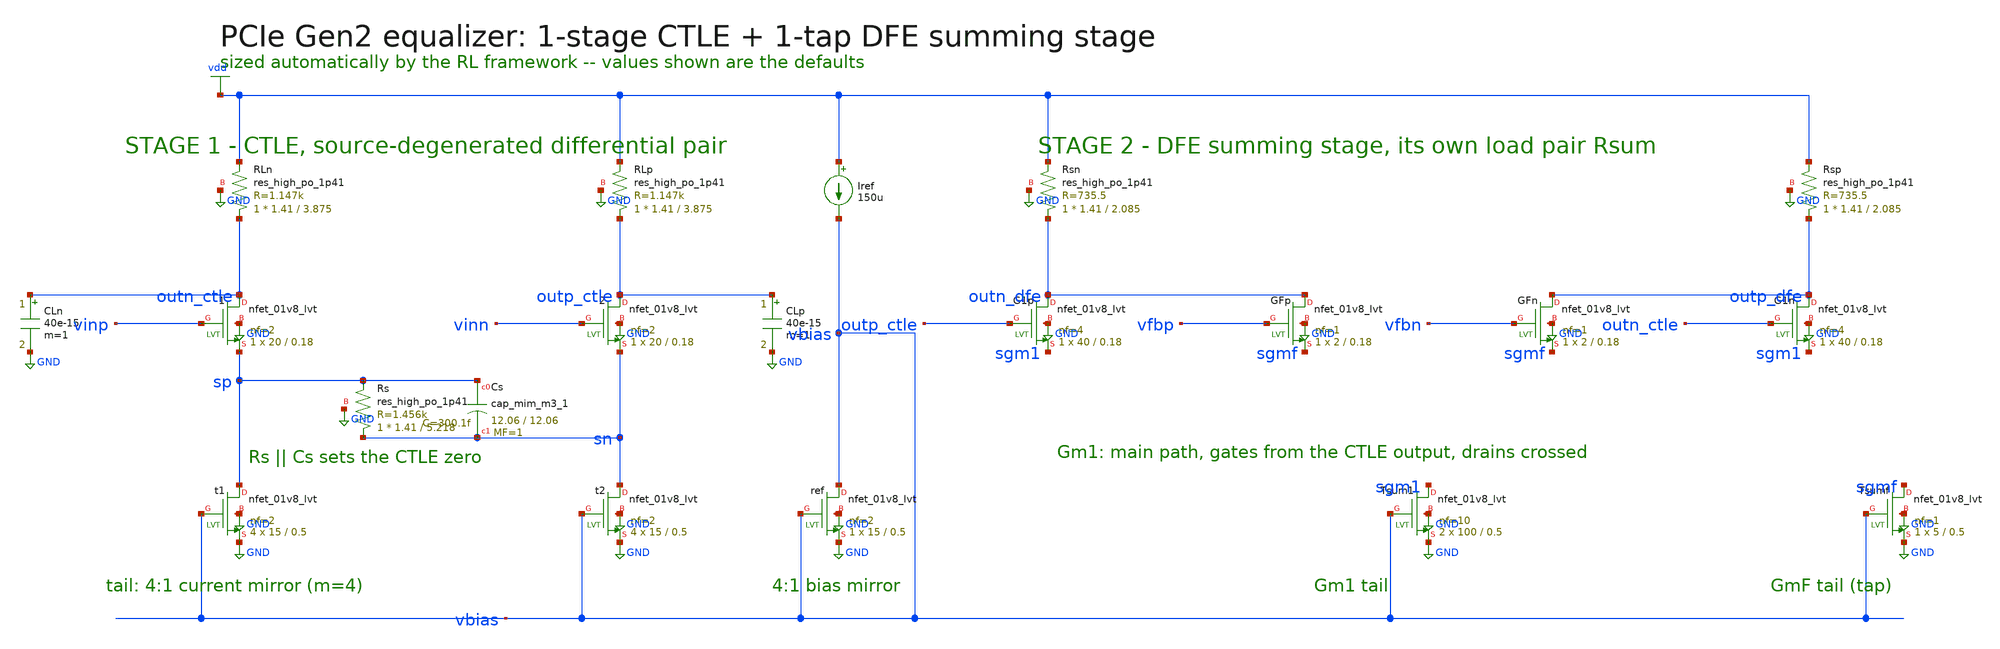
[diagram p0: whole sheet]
** sch_path: netlists/eq_core.sch
**.subckt eq_core
XRLn outn_ctle vdd GND sky130_fd_pr__res_high_po_1p41 L=3.875 mult=1 m=1
XRLp outp_ctle vdd GND sky130_fd_pr__res_high_po_1p41 L=3.875 mult=1 m=1
X1 outn_ctle vinp sp GND sky130_fd_pr__nfet_01v8_lvt L=0.18 W=20 nf=2 ad=0 as=0 pd=0 ps=0 nrd=0
+ nrs=0 sa=0 sb=0 sd=0 mult=1 m=1
X2 outp_ctle vinn sn GND sky130_fd_pr__nfet_01v8_lvt L=0.18 W=20 nf=2 ad=0 as=0 pd=0 ps=0 nrd=0
+ nrs=0 sa=0 sb=0 sd=0 mult=1 m=1
CLn outn_ctle GND 40e-15 m=1
CLp outp_ctle GND 40e-15 m=1
Xt1 sp vbias GND GND sky130_fd_pr__nfet_01v8_lvt L=0.5 W=15 nf=2 ad=0 as=0 pd=0 ps=0 nrd=0 nrs=0
+ sa=0 sb=0 sd=0 mult=4 m=4
Xt2 sn vbias GND GND sky130_fd_pr__nfet_01v8_lvt L=0.5 W=15 nf=2 ad=0 as=0 pd=0 ps=0 nrd=0 nrs=0
+ sa=0 sb=0 sd=0 mult=4 m=4
XRs sn sp GND sky130_fd_pr__res_high_po_1p41 L=5.218 mult=1 m=1
XCs sp sn sky130_fd_pr__cap_mim_m3_1 W=12.06 L=12.06 MF=1 m=1
Iref vdd vbias 150u
Xref vbias vbias GND GND sky130_fd_pr__nfet_01v8_lvt L=0.5 W=15 nf=2 ad=0 as=0 pd=0 ps=0 nrd=0 nrs=0
+ sa=0 sb=0 sd=0 mult=1 m=1
XRsn outn_dfe vdd GND sky130_fd_pr__res_high_po_1p41 L=2.085 mult=1 m=1
XRsp outp_dfe vdd GND sky130_fd_pr__res_high_po_1p41 L=2.085 mult=1 m=1
XG1p outn_dfe outp_ctle sgm1 GND sky130_fd_pr__nfet_01v8_lvt L=0.18 W=40 nf=4 ad=0 as=0 pd=0 ps=0
+ nrd=0 nrs=0 sa=0 sb=0 sd=0 mult=1 m=1
XG1n outp_dfe outn_ctle sgm1 GND sky130_fd_pr__nfet_01v8_lvt L=0.18 W=40 nf=4 ad=0 as=0 pd=0 ps=0
+ nrd=0 nrs=0 sa=0 sb=0 sd=0 mult=1 m=1
XGFp outn_dfe vfbp sgmf GND sky130_fd_pr__nfet_01v8_lvt L=0.18 W=2 nf=1 ad=0 as=0 pd=0 ps=0 nrd=0
+ nrs=0 sa=0 sb=0 sd=0 mult=1 m=1
XGFn outp_dfe vfbn sgmf GND sky130_fd_pr__nfet_01v8_lvt L=0.18 W=2 nf=1 ad=0 as=0 pd=0 ps=0 nrd=0
+ nrs=0 sa=0 sb=0 sd=0 mult=1 m=1
XTsum1 sgm1 vbias GND GND sky130_fd_pr__nfet_01v8_lvt L=0.5 W=100 nf=10 ad=0 as=0 pd=0 ps=0 nrd=0
+ nrs=0 sa=0 sb=0 sd=0 mult=2 m=2
XTsumf sgmf vbias GND GND sky130_fd_pr__nfet_01v8_lvt L=0.5 W=5 nf=1 ad=0 as=0 pd=0 ps=0 nrd=0 nrs=0
+ sa=0 sb=0 sd=0 mult=1 m=1
**.ends
.GLOBAL GND
.GLOBAL vdd
.end
